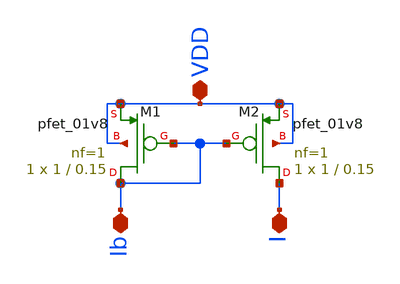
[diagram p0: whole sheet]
** sch_path: mirror_current/mirror_current.sch
**.subckt mirror_current VDD Ib I
*.iopin VDD
*.iopin Ib
*.iopin I
XM1 Ib Ib VDD VDD sky130_fd_pr__pfet_01v8 L=0.15 W=1 nf=1 ad='int((nf+1)/2) * W/nf * 0.29' as='int((nf+2)/2) * W/nf * 0.29'
+ pd='2*int((nf+1)/2) * (W/nf + 0.29)' ps='2*int((nf+2)/2) * (W/nf + 0.29)' nrd='0.29 / W' nrs='0.29 / W'
+ sa=0 sb=0 sd=0 mult=1 m=1
XM2 I Ib VDD VDD sky130_fd_pr__pfet_01v8 L=0.15 W=1 nf=1 ad='int((nf+1)/2) * W/nf * 0.29' as='int((nf+2)/2) * W/nf * 0.29'
+ pd='2*int((nf+1)/2) * (W/nf + 0.29)' ps='2*int((nf+2)/2) * (W/nf + 0.29)' nrd='0.29 / W' nrs='0.29 / W'
+ sa=0 sb=0 sd=0 mult=1 m=1
**.ends
.end
